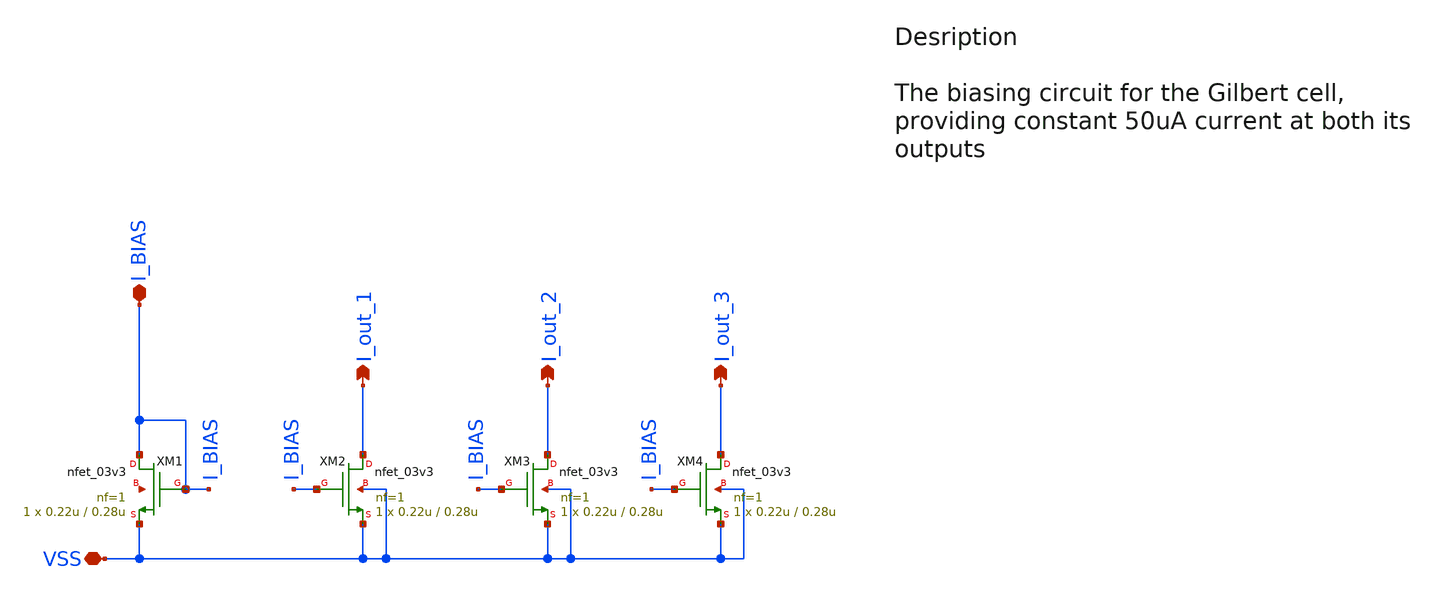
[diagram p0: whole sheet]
** sch_path: designs/libs/core_top/A5_Time_Transcenders/schematics/Biasing_network_no_hierarchy.sch
**.subckt Biasing_network_no_hierarchy VSS I_BIAS I_out_1 I_out_2 I_out_3
*.iopin VSS
*.iopin I_BIAS
*.opin I_out_1
*.opin I_out_2
*.opin I_out_3
XM1 I_BIAS I_BIAS VSS net1 nfet_03v3 L=0.28u W=0.22u nf=1 ad='int((nf+1)/2) * W/nf * 0.18u' as='int((nf+2)/2) * W/nf * 0.18u'
+ pd='2*int((nf+1)/2) * (W/nf + 0.18u)' ps='2*int((nf+2)/2) * (W/nf + 0.18u)' nrd='0.18u / W' nrs='0.18u / W'
+ sa=0 sb=0 sd=0 m=1
XM2 I_out_1 I_BIAS VSS VSS nfet_03v3 L=0.28u W=0.22u nf=1 ad='int((nf+1)/2) * W/nf * 0.18u' as='int((nf+2)/2) * W/nf * 0.18u'
+ pd='2*int((nf+1)/2) * (W/nf + 0.18u)' ps='2*int((nf+2)/2) * (W/nf + 0.18u)' nrd='0.18u / W' nrs='0.18u / W'
+ sa=0 sb=0 sd=0 m=1
XM3 I_out_2 I_BIAS VSS VSS nfet_03v3 L=0.28u W=0.22u nf=1 ad='int((nf+1)/2) * W/nf * 0.18u' as='int((nf+2)/2) * W/nf * 0.18u'
+ pd='2*int((nf+1)/2) * (W/nf + 0.18u)' ps='2*int((nf+2)/2) * (W/nf + 0.18u)' nrd='0.18u / W' nrs='0.18u / W'
+ sa=0 sb=0 sd=0 m=1
XM4 I_out_3 I_BIAS VSS VSS nfet_03v3 L=0.28u W=0.22u nf=1 ad='int((nf+1)/2) * W/nf * 0.18u' as='int((nf+2)/2) * W/nf * 0.18u'
+ pd='2*int((nf+1)/2) * (W/nf + 0.18u)' ps='2*int((nf+2)/2) * (W/nf + 0.18u)' nrd='0.18u / W' nrs='0.18u / W'
+ sa=0 sb=0 sd=0 m=1
**** begin user architecture code

.include $::180MCU_MODELS/design.ngspice
.lib $::180MCU_MODELS/sm141064.ngspice typical
.lib $::180MCU_MODELS/sm141064.ngspice mimcap_typical
.lib $::180MCU_MODELS/sm141064.ngspice cap_mim
.lib $::180MCU_MODELS/sm141064.ngspice res_typical




* let sets vectors to a plot, while set sets a variable, globally accessible in .control
.control

    * Set frequency and amplitude variables to proper values from within the control sequence
    save all

    op
    show

    write Biasing_network_sim.raw

    set appendwrite

    * Transient analysis to observe mixing operation
    tran 1p 10n


    write Biasing_network_sim.raw

.endc


**** end user architecture code
**.ends
.end
